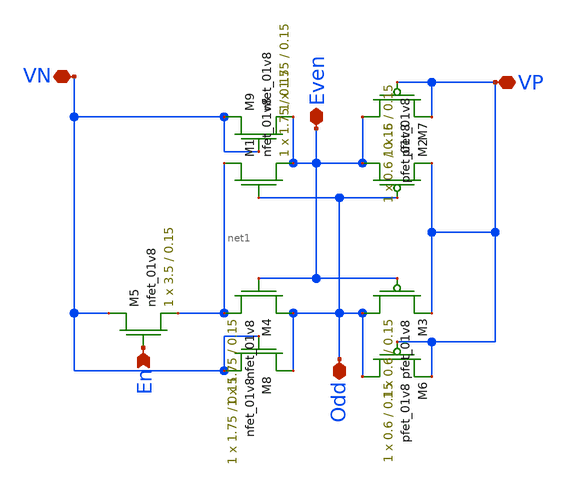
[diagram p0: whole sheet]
** sch_path: DRAM_Components/Schematic/SenseAmp.sch
**.subckt SenseAmp Odd En VN VP Even
*.iopin Odd
*.ipin En
*.iopin VN
*.iopin VP
*.iopin Even
XM1 net1 Odd Even VN sky130_fd_pr__nfet_01v8 L=0.15 W=1.75 nf=1 ad='int((nf+1)/2) * W/nf * 0.29' as='int((nf+2)/2) * W/nf * 0.29'
+ pd='2*int((nf+1)/2) * (W/nf + 0.29)' ps='2*int((nf+2)/2) * (W/nf + 0.29)' nrd='0.29 / W' nrs='0.29 / W'
+ sa=0 sb=0 sd=0 mult=1 m=1
XM2 Even Odd VP VP sky130_fd_pr__pfet_01v8 L=0.15 W=.6 nf=1 ad='int((nf+1)/2) * W/nf * 0.29' as='int((nf+2)/2) * W/nf * 0.29'
+ pd='2*int((nf+1)/2) * (W/nf + 0.29)' ps='2*int((nf+2)/2) * (W/nf + 0.29)' nrd='0.29 / W' nrs='0.29 / W'
+ sa=0 sb=0 sd=0 mult=1 m=1
XM3 Odd Even VP VP sky130_fd_pr__pfet_01v8 L=0.15 W=0.6 nf=1 ad='int((nf+1)/2) * W/nf * 0.29' as='int((nf+2)/2) * W/nf * 0.29'
+ pd='2*int((nf+1)/2) * (W/nf + 0.29)' ps='2*int((nf+2)/2) * (W/nf + 0.29)' nrd='0.29 / W' nrs='0.29 / W'
+ sa=0 sb=0 sd=0 mult=1 m=1
XM4 Odd Even net1 VN sky130_fd_pr__nfet_01v8 L=0.15 W=1.75 nf=1 ad='int((nf+1)/2) * W/nf * 0.29' as='int((nf+2)/2) * W/nf * 0.29'
+ pd='2*int((nf+1)/2) * (W/nf + 0.29)' ps='2*int((nf+2)/2) * (W/nf + 0.29)' nrd='0.29 / W' nrs='0.29 / W'
+ sa=0 sb=0 sd=0 mult=1 m=1
XM5 VN En net1 VN sky130_fd_pr__nfet_01v8 L=0.15 W=3.5 nf=1 ad='int((nf+1)/2) * W/nf * 0.29' as='int((nf+2)/2) * W/nf * 0.29'
+ pd='2*int((nf+1)/2) * (W/nf + 0.29)' ps='2*int((nf+2)/2) * (W/nf + 0.29)' nrd='0.29 / W' nrs='0.29 / W'
+ sa=0 sb=0 sd=0 mult=1 m=1
XM6 Odd VP VP VP sky130_fd_pr__pfet_01v8 L=0.15 W=0.6 nf=1 ad='int((nf+1)/2) * W/nf * 0.29' as='int((nf+2)/2) * W/nf * 0.29'
+ pd='2*int((nf+1)/2) * (W/nf + 0.29)' ps='2*int((nf+2)/2) * (W/nf + 0.29)' nrd='0.29 / W' nrs='0.29 / W'
+ sa=0 sb=0 sd=0 mult=1 m=1
XM7 Even VP VP VP sky130_fd_pr__pfet_01v8 L=0.15 W=0.6 nf=1 ad='int((nf+1)/2) * W/nf * 0.29' as='int((nf+2)/2) * W/nf * 0.29'
+ pd='2*int((nf+1)/2) * (W/nf + 0.29)' ps='2*int((nf+2)/2) * (W/nf + 0.29)' nrd='0.29 / W' nrs='0.29 / W'
+ sa=0 sb=0 sd=0 mult=1 m=1
XM8 Odd VN VN VN sky130_fd_pr__nfet_01v8 L=0.15 W=1.75 nf=1 ad='int((nf+1)/2) * W/nf * 0.29' as='int((nf+2)/2) * W/nf * 0.29'
+ pd='2*int((nf+1)/2) * (W/nf + 0.29)' ps='2*int((nf+2)/2) * (W/nf + 0.29)' nrd='0.29 / W' nrs='0.29 / W'
+ sa=0 sb=0 sd=0 mult=1 m=1
XM9 VN VN Even VN sky130_fd_pr__nfet_01v8 L=0.15 W=1.75 nf=1 ad='int((nf+1)/2) * W/nf * 0.29' as='int((nf+2)/2) * W/nf * 0.29'
+ pd='2*int((nf+1)/2) * (W/nf + 0.29)' ps='2*int((nf+2)/2) * (W/nf + 0.29)' nrd='0.29 / W' nrs='0.29 / W'
+ sa=0 sb=0 sd=0 mult=1 m=1
**.ends
.end
